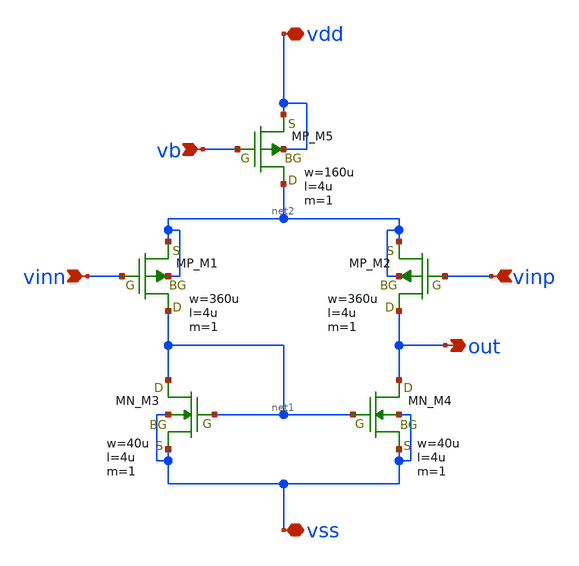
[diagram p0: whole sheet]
** sch_path: member_project/opamp/july_fifth/diff.sch
**.subckt diff vinn vinp vb out vdd vss
*.ipin vinn
*.ipin vinp
*.ipin vb
*.opin out
*.iopin vdd
*.iopin vss
XM5 net2 vb vdd vdd PMOS w=160u l=4u as=0 ad=0 ps=0 pd=0 nrd=0 nrs=0 m=1
XM1 net1 vinn net2 net2 PMOS w=360u l=4u as=0 ad=0 ps=0 pd=0 nrd=0 nrs=0 m=1
XM2 out vinp net2 net2 PMOS w=360u l=4u as=0 ad=0 ps=0 pd=0 nrd=0 nrs=0 m=1
XM3 net1 net1 vss vss NMOS w=40u l=4u as=0 ad=0 ps=0 pd=0 nrd=0 nrs=0 m=1
XM4 out net1 vss vss NMOS w=40u l=4u as=0 ad=0 ps=0 pd=0 nrd=0 nrs=0 m=1
**.ends
.end
